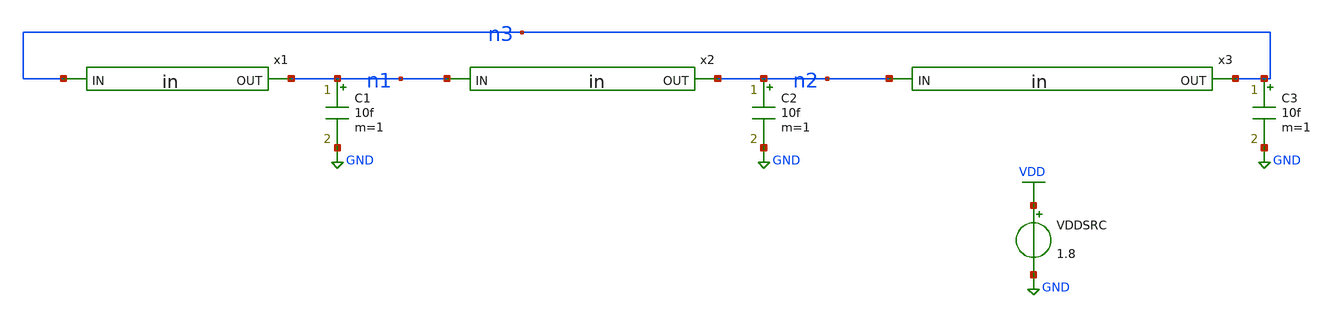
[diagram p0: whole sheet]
** sch_path: ring3.sch
**.subckt ring3
x1 n3 n1 in
x2 n1 n2 in
x3 n2 n3 in
VDDSRC VDD GND 1.8
C1 n1 GND 10f m=1
C2 n2 GND 10f m=1
C3 n3 GND 10f m=1
**** begin user architecture code

.lib /home/devesh/vlsi_tools/open_pdks/sky130/sky130A/libs.tech/ngspice/sky130.lib.spice fs

.ic V(n1)=1.8 V(n2)=0 V(n3)=0
.temp 27


.control
tran 1p 10n uic
run

meas tran period TRIG v(n1) VAL=0.9 RISE=5 TARG v(n1) VAL=0.9 RISE=6
let freq = 1/period

print period
print freq

plot v(n1)
.endc

**** end user architecture code
**.ends
.GLOBAL VDD
.GLOBAL GND
.end
